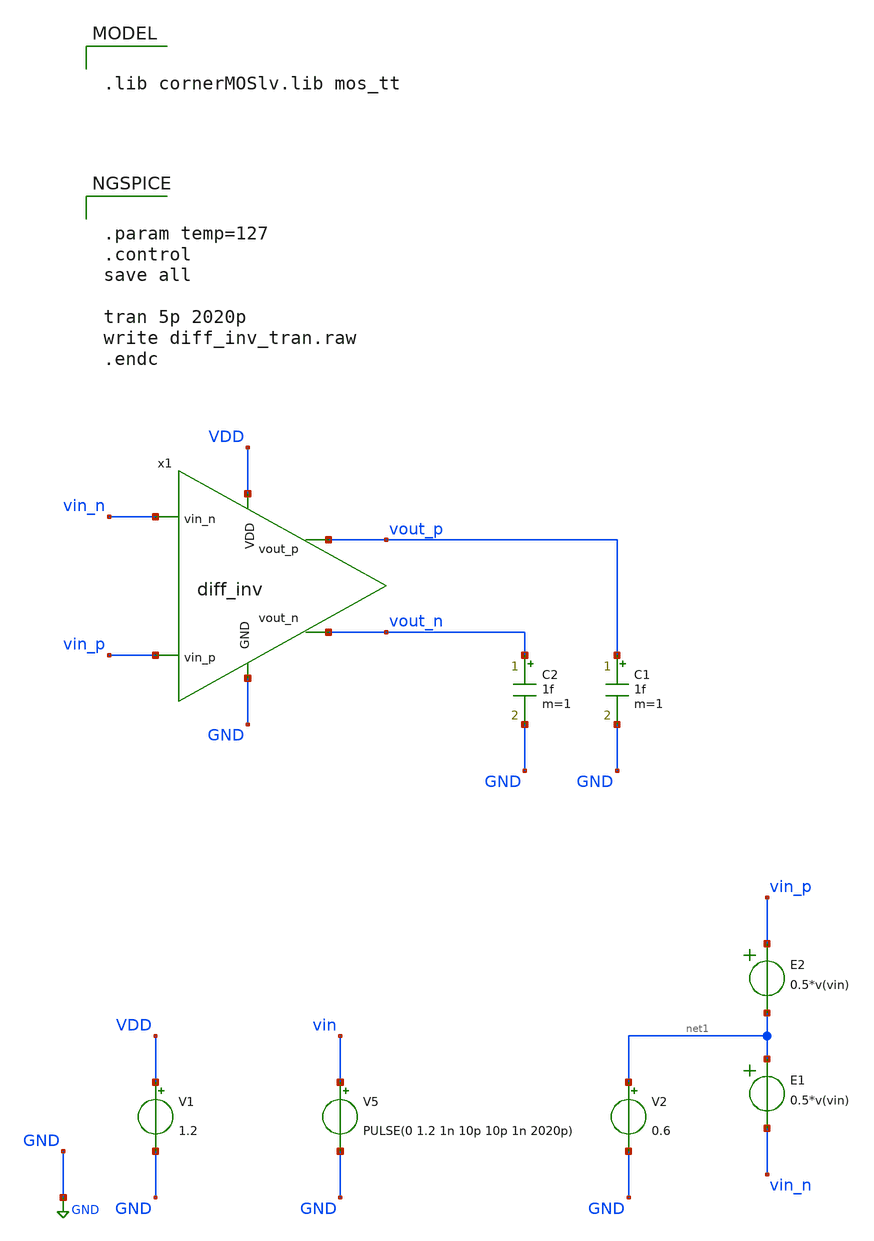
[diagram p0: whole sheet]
** sch_path: 20260718_ring_oscillator/diff_inv_tb.sch
**.subckt diff_inv_tb
x1 vin_n vin_p vout_n vout_p VDD GND diff_inv
V1 VDD GND 1.2
C1 vout_p GND 1f m=1
C2 vout_n GND 1f m=1
V2 net1 GND 0.6
V5 vin GND PULSE(0 1.2 1n 10p 10p 1n 2020p)
E1 net1 vin_n VOL=' 0.5*v(vin) '
E2 vin_p net1 VOL=' 0.5*v(vin) '
**** begin user architecture code

.lib cornerMOSlv.lib mos_tt



.param temp=127
.control
save all

tran 5p 2020p
write diff_inv_tran.raw
.endc


**** end user architecture code
**.ends

* expanding   symbol:  diff_inv.sym # of pins=6
** sym_path: 20260718_ring_oscillator/diff_inv.sym
** sch_path: 20260718_ring_oscillator/diff_inv.sch
.subckt diff_inv vin_n vin_p vout_n vout_p VDD GND
*.opin vout_p
*.iopin VDD
*.iopin GND
*.opin vout_n
*.ipin vin_p
*.ipin vin_n
XM1 vout_p vin_n net1 net1 sg13_lv_nmos w=1.5u l=0.13u ng=1 m=1 mm_ok=1
XM2 vout_n vin_p net1 net1 sg13_lv_nmos w=1.5u l=0.13u ng=1 m=1 mm_ok=1
R1 VDD vout_p 1k m=1
R2 VDD vout_n 1k m=1
I0 net1 GND 1m
.ends

.GLOBAL GND
.end
